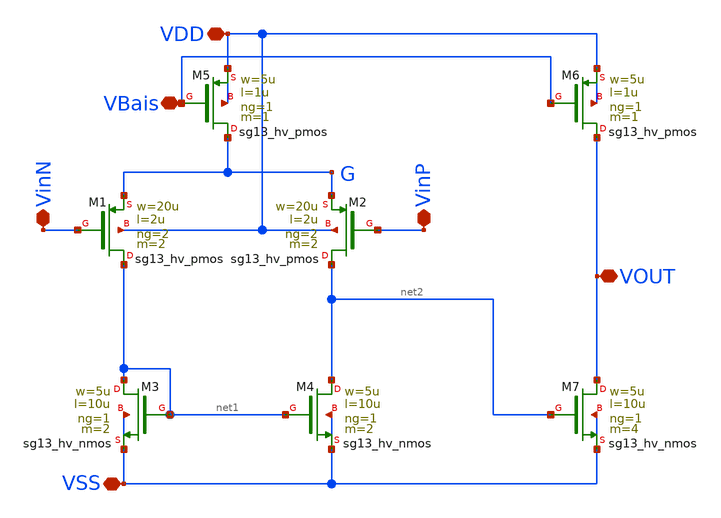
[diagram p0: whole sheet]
** sch_path: xschem/Comp_2Stage.sch
**.subckt Comp_2Stage VDD VBais VinP VinN VOUT VSS
*.iopin VDD
*.iopin VBais
*.iopin VinP
*.iopin VinN
*.iopin VOUT
*.iopin VSS
XM3 net1 net1 VSS VSS sg13_hv_nmos w=5u l=10u ng=1 m=2 mm_ok=1
XM1 net1 VinN G VDD sg13_hv_pmos w=20u l=2u ng=2 m=2 mm_ok=1
XM2 net2 VinP G VDD sg13_hv_pmos w=20u l=2u ng=2 m=2 mm_ok=1
XM4 net2 net1 VSS VSS sg13_hv_nmos w=5u l=10u ng=1 m=2 mm_ok=1
XM5 G VBais VDD VDD sg13_hv_pmos w=5u l=1u ng=1 m=1 mm_ok=1
XM6 VOUT VBais VDD VDD sg13_hv_pmos w=5u l=1u ng=1 m=1 mm_ok=1
XM7 VOUT net2 VSS VSS sg13_hv_nmos w=5u l=10u ng=1 m=4 mm_ok=1
**.ends
.end
